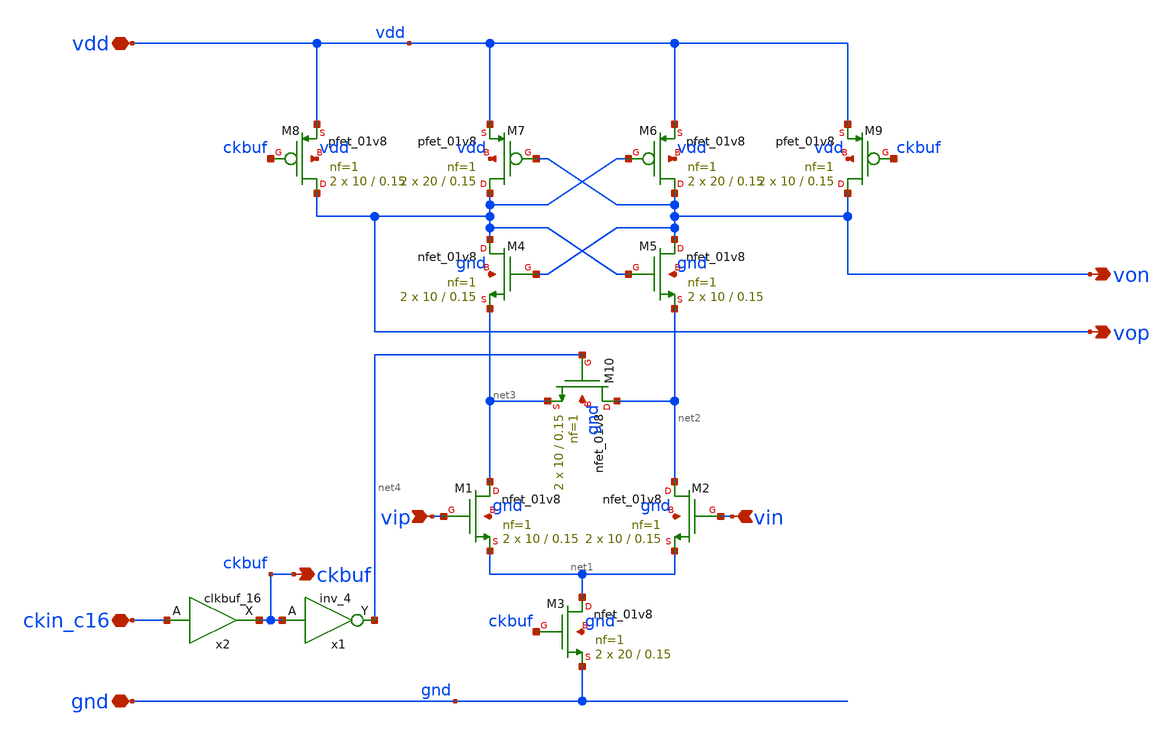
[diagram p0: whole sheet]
** sch_path: xschem/adc_strongarm.sch
**.subckt adc_strongarm vip vin gnd vdd vop von ckin_c16 ckbuf
*.ipin vip
*.ipin vin
*.iopin gnd
*.iopin vdd
*.opin vop
*.opin von
*.iopin ckin_c16
*.opin ckbuf
XM1 net3 vip net1 gnd sky130_fd_pr__nfet_01v8 L=0.15 W=10 nf=1 ad='int((nf+1)/2) * W/nf * 0.29' as='int((nf+2)/2) * W/nf * 0.29'
+ pd='2*int((nf+1)/2) * (W/nf + 0.29)' ps='2*int((nf+2)/2) * (W/nf + 0.29)' nrd='0.29 / W' nrs='0.29 / W'
+ sa=0 sb=0 sd=0 mult=2 m=2
XM2 net2 vin net1 gnd sky130_fd_pr__nfet_01v8 L=0.15 W=10 nf=1 ad='int((nf+1)/2) * W/nf * 0.29' as='int((nf+2)/2) * W/nf * 0.29'
+ pd='2*int((nf+1)/2) * (W/nf + 0.29)' ps='2*int((nf+2)/2) * (W/nf + 0.29)' nrd='0.29 / W' nrs='0.29 / W'
+ sa=0 sb=0 sd=0 mult=2 m=2
XM3 net1 ckbuf gnd gnd sky130_fd_pr__nfet_01v8 L=0.15 W=20 nf=1 ad='int((nf+1)/2) * W/nf * 0.29' as='int((nf+2)/2) * W/nf * 0.29'
+ pd='2*int((nf+1)/2) * (W/nf + 0.29)' ps='2*int((nf+2)/2) * (W/nf + 0.29)' nrd='0.29 / W' nrs='0.29 / W'
+ sa=0 sb=0 sd=0 mult=2 m=2
XM4 vop von net3 gnd sky130_fd_pr__nfet_01v8 L=0.15 W=10 nf=1 ad='int((nf+1)/2) * W/nf * 0.29' as='int((nf+2)/2) * W/nf * 0.29'
+ pd='2*int((nf+1)/2) * (W/nf + 0.29)' ps='2*int((nf+2)/2) * (W/nf + 0.29)' nrd='0.29 / W' nrs='0.29 / W'
+ sa=0 sb=0 sd=0 mult=2 m=2
XM5 von vop net2 gnd sky130_fd_pr__nfet_01v8 L=0.15 W=10 nf=1 ad='int((nf+1)/2) * W/nf * 0.29' as='int((nf+2)/2) * W/nf * 0.29'
+ pd='2*int((nf+1)/2) * (W/nf + 0.29)' ps='2*int((nf+2)/2) * (W/nf + 0.29)' nrd='0.29 / W' nrs='0.29 / W'
+ sa=0 sb=0 sd=0 mult=2 m=2
XM6 von vop vdd vdd sky130_fd_pr__pfet_01v8 L=0.15 W=20 nf=1 ad='int((nf+1)/2) * W/nf * 0.29' as='int((nf+2)/2) * W/nf * 0.29'
+ pd='2*int((nf+1)/2) * (W/nf + 0.29)' ps='2*int((nf+2)/2) * (W/nf + 0.29)' nrd='0.29 / W' nrs='0.29 / W'
+ sa=0 sb=0 sd=0 mult=2 m=2
XM7 vop von vdd vdd sky130_fd_pr__pfet_01v8 L=0.15 W=20 nf=1 ad='int((nf+1)/2) * W/nf * 0.29' as='int((nf+2)/2) * W/nf * 0.29'
+ pd='2*int((nf+1)/2) * (W/nf + 0.29)' ps='2*int((nf+2)/2) * (W/nf + 0.29)' nrd='0.29 / W' nrs='0.29 / W'
+ sa=0 sb=0 sd=0 mult=2 m=2
XM8 vop ckbuf vdd vdd sky130_fd_pr__pfet_01v8 L=0.15 W=10 nf=1 ad='int((nf+1)/2) * W/nf * 0.29' as='int((nf+2)/2) * W/nf * 0.29'
+ pd='2*int((nf+1)/2) * (W/nf + 0.29)' ps='2*int((nf+2)/2) * (W/nf + 0.29)' nrd='0.29 / W' nrs='0.29 / W'
+ sa=0 sb=0 sd=0 mult=2 m=2
XM9 von ckbuf vdd vdd sky130_fd_pr__pfet_01v8 L=0.15 W=10 nf=1 ad='int((nf+1)/2) * W/nf * 0.29' as='int((nf+2)/2) * W/nf * 0.29'
+ pd='2*int((nf+1)/2) * (W/nf + 0.29)' ps='2*int((nf+2)/2) * (W/nf + 0.29)' nrd='0.29 / W' nrs='0.29 / W'
+ sa=0 sb=0 sd=0 mult=2 m=2
x1 ckbuf gnd gnd vdd vdd net4 sky130_fd_sc_hs__inv_4
XM10 net2 net4 net3 gnd sky130_fd_pr__nfet_01v8 L=0.15 W=10 nf=1 ad='int((nf+1)/2) * W/nf * 0.29' as='int((nf+2)/2) * W/nf * 0.29'
+ pd='2*int((nf+1)/2) * (W/nf + 0.29)' ps='2*int((nf+2)/2) * (W/nf + 0.29)' nrd='0.29 / W' nrs='0.29 / W'
+ sa=0 sb=0 sd=0 mult=2 m=2
x2 ckin_c16 gnd gnd vdd vdd ckbuf sky130_fd_sc_hs__clkbuf_16
**.ends
.end
